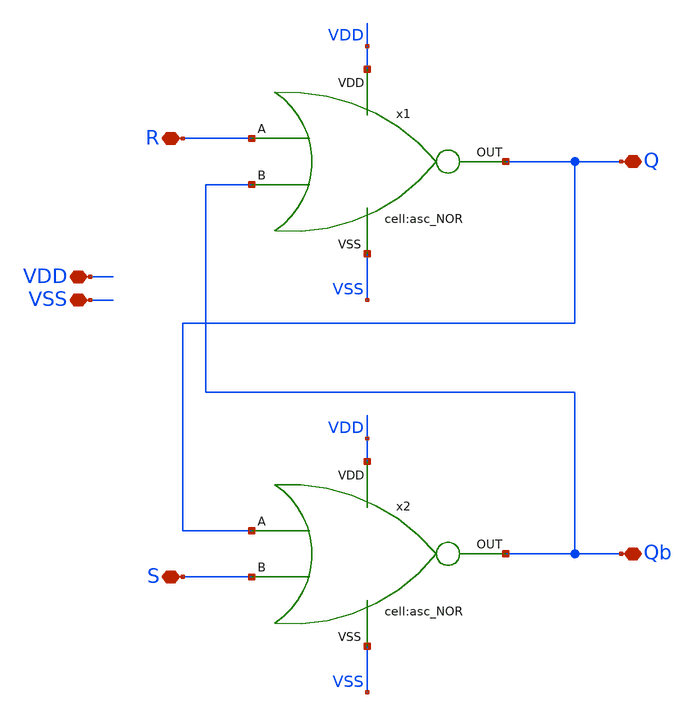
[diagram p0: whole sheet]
** sch_path: designs/libs/xp_core_analog/asc_SR_latch/asc_SR_latch.sch
**.subckt asc_SR_latch VDD VSS S R Qb Q
*.iopin VDD
*.iopin VSS
*.iopin S
*.iopin R
*.iopin Qb
*.iopin Q
x1 VDD VSS Q R Qb asc_NOR
x2 VDD VSS Qb Q S asc_NOR
**.ends

* expanding   symbol:  libs/core_analog/asc_NOR/asc_NOR.sym # of pins=5
** sym_path: designs/libs/xp_core_analog/asc_NOR/asc_NOR.sym
** sch_path: designs/libs/xp_core_analog/asc_NOR/asc_NOR.sch
.subckt asc_NOR VDD VSS OUT A B
*.iopin VDD
*.iopin VSS
*.iopin B
*.iopin A
*.iopin OUT
XM1 OUT A VSS VSS nfet_03v3 L=0.5u W=1u nf=1 ad='int((nf+1)/2) * W/nf * 0.18u' as='int((nf+2)/2) * W/nf * 0.18u'
+ pd='2*int((nf+1)/2) * (W/nf + 0.18u)' ps='2*int((nf+2)/2) * (W/nf + 0.18u)' nrd='0.18u / W' nrs='0.18u / W'
+ sa=0 sb=0 sd=0 m=1
XM2 OUT B VSS VSS nfet_03v3 L=0.5u W=1u nf=1 ad='int((nf+1)/2) * W/nf * 0.18u' as='int((nf+2)/2) * W/nf * 0.18u'
+ pd='2*int((nf+1)/2) * (W/nf + 0.18u)' ps='2*int((nf+2)/2) * (W/nf + 0.18u)' nrd='0.18u / W' nrs='0.18u / W'
+ sa=0 sb=0 sd=0 m=1
XM3 OUT B net1 VDD pfet_03v3 L=0.5u W=1u nf=6 ad='int((nf+1)/2) * W/nf * 0.18u' as='int((nf+2)/2) * W/nf * 0.18u'
+ pd='2*int((nf+1)/2) * (W/nf + 0.18u)' ps='2*int((nf+2)/2) * (W/nf + 0.18u)' nrd='0.18u / W' nrs='0.18u / W'
+ sa=0 sb=0 sd=0 m=1
XM4 net1 A VDD VDD pfet_03v3 L=0.5u W=1u nf=6 ad='int((nf+1)/2) * W/nf * 0.18u' as='int((nf+2)/2) * W/nf * 0.18u'
+ pd='2*int((nf+1)/2) * (W/nf + 0.18u)' ps='2*int((nf+2)/2) * (W/nf + 0.18u)' nrd='0.18u / W' nrs='0.18u / W'
+ sa=0 sb=0 sd=0 m=1
.ends

.end
